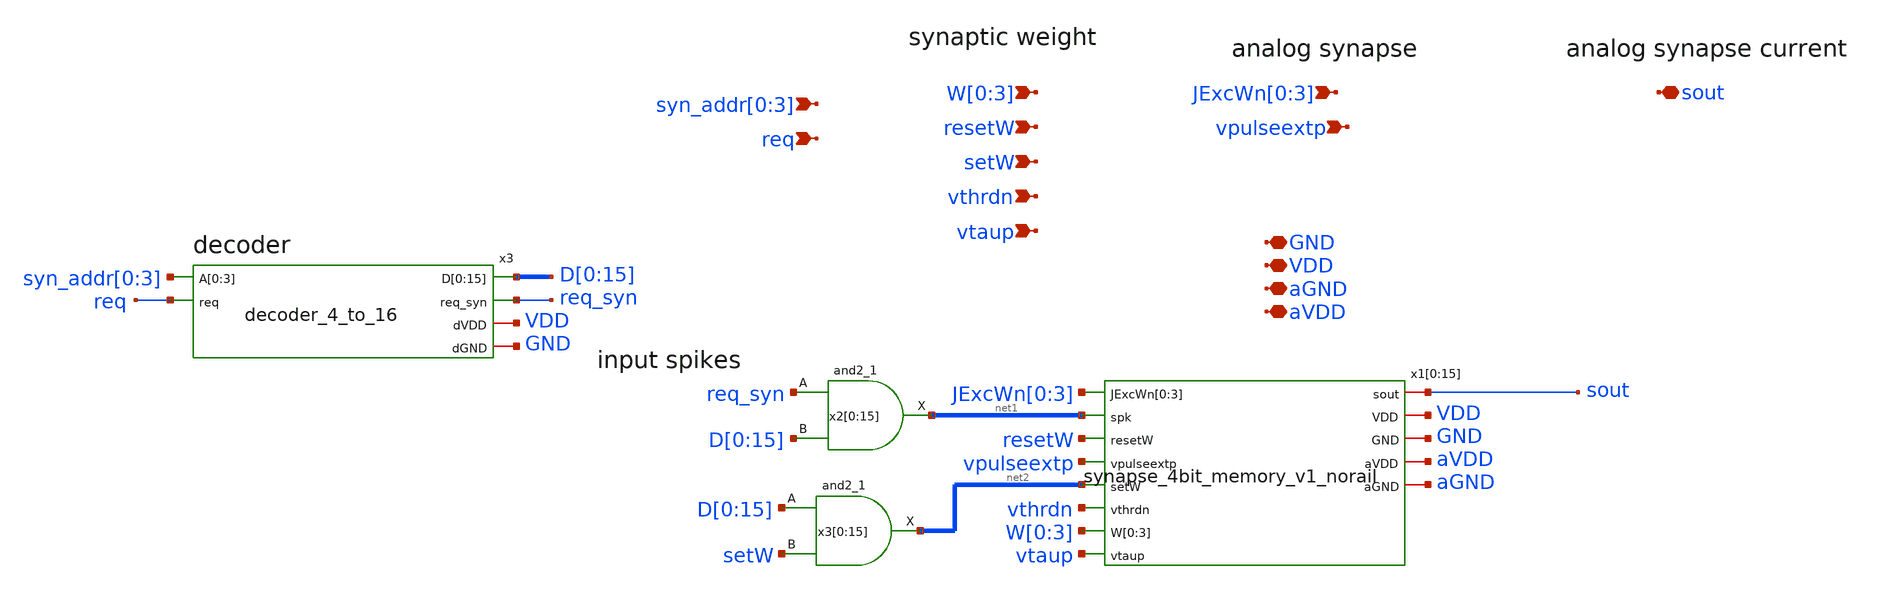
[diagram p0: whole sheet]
** sch_path: design/xschem/synapse_array_programmable_16_to_sout_v1.sch
**.subckt synapse_array_programmable_16_to_sout_v1 GND VDD vpulseextp
*+ syn_addr[0],syn_addr[1],syn_addr[2],syn_addr[3] W[0],W[1],W[2],W[3] JExcWn[0],JExcWn[1],JExcWn[2],JExcWn[3] sout setW resetW req vthrdn vtaup aVDD
*+ aGND
*.iopin GND
*.iopin VDD
*.ipin vpulseextp
*.ipin syn_addr[0],syn_addr[1],syn_addr[2],syn_addr[3]
*.ipin W[0],W[1],W[2],W[3]
*.ipin JExcWn[0],JExcWn[1],JExcWn[2],JExcWn[3]
*.iopin sout
*.ipin setW
*.ipin resetW
*.ipin req
*.ipin vthrdn
*.ipin vtaup
*.iopin aVDD
*.iopin aGND
x3 syn_addr[0] syn_addr[1] syn_addr[2] syn_addr[3] D[0] D[1] D[2] D[3] D[4] D[5] D[6] D[7] D[8] D[9]
+ D[10] D[11] D[12] D[13] D[14] D[15] req req_syn VDD GND decoder_4_to_16
x2[0] req_syn D[0] GND GND VDD VDD net1[15] sky130_fd_sc_hd__and2_1
x2[1] req_syn D[1] GND GND VDD VDD net1[14] sky130_fd_sc_hd__and2_1
x2[2] req_syn D[2] GND GND VDD VDD net1[13] sky130_fd_sc_hd__and2_1
x2[3] req_syn D[3] GND GND VDD VDD net1[12] sky130_fd_sc_hd__and2_1
x2[4] req_syn D[4] GND GND VDD VDD net1[11] sky130_fd_sc_hd__and2_1
x2[5] req_syn D[5] GND GND VDD VDD net1[10] sky130_fd_sc_hd__and2_1
x2[6] req_syn D[6] GND GND VDD VDD net1[9] sky130_fd_sc_hd__and2_1
x2[7] req_syn D[7] GND GND VDD VDD net1[8] sky130_fd_sc_hd__and2_1
x2[8] req_syn D[8] GND GND VDD VDD net1[7] sky130_fd_sc_hd__and2_1
x2[9] req_syn D[9] GND GND VDD VDD net1[6] sky130_fd_sc_hd__and2_1
x2[10] req_syn D[10] GND GND VDD VDD net1[5] sky130_fd_sc_hd__and2_1
x2[11] req_syn D[11] GND GND VDD VDD net1[4] sky130_fd_sc_hd__and2_1
x2[12] req_syn D[12] GND GND VDD VDD net1[3] sky130_fd_sc_hd__and2_1
x2[13] req_syn D[13] GND GND VDD VDD net1[2] sky130_fd_sc_hd__and2_1
x2[14] req_syn D[14] GND GND VDD VDD net1[1] sky130_fd_sc_hd__and2_1
x2[15] req_syn D[15] GND GND VDD VDD net1[0] sky130_fd_sc_hd__and2_1
x1[0] sout JExcWn[0] JExcWn[1] JExcWn[2] JExcWn[3] net1[15] resetW vpulseextp net2[15] vthrdn W[0]
+ W[1] W[2] W[3] vtaup VDD GND aVDD aGND synapse_4bit_memory_v1_norail
x1[1] sout JExcWn[0] JExcWn[1] JExcWn[2] JExcWn[3] net1[14] resetW vpulseextp net2[14] vthrdn W[0]
+ W[1] W[2] W[3] vtaup VDD GND aVDD aGND synapse_4bit_memory_v1_norail
x1[2] sout JExcWn[0] JExcWn[1] JExcWn[2] JExcWn[3] net1[13] resetW vpulseextp net2[13] vthrdn W[0]
+ W[1] W[2] W[3] vtaup VDD GND aVDD aGND synapse_4bit_memory_v1_norail
x1[3] sout JExcWn[0] JExcWn[1] JExcWn[2] JExcWn[3] net1[12] resetW vpulseextp net2[12] vthrdn W[0]
+ W[1] W[2] W[3] vtaup VDD GND aVDD aGND synapse_4bit_memory_v1_norail
x1[4] sout JExcWn[0] JExcWn[1] JExcWn[2] JExcWn[3] net1[11] resetW vpulseextp net2[11] vthrdn W[0]
+ W[1] W[2] W[3] vtaup VDD GND aVDD aGND synapse_4bit_memory_v1_norail
x1[5] sout JExcWn[0] JExcWn[1] JExcWn[2] JExcWn[3] net1[10] resetW vpulseextp net2[10] vthrdn W[0]
+ W[1] W[2] W[3] vtaup VDD GND aVDD aGND synapse_4bit_memory_v1_norail
x1[6] sout JExcWn[0] JExcWn[1] JExcWn[2] JExcWn[3] net1[9] resetW vpulseextp net2[9] vthrdn W[0]
+ W[1] W[2] W[3] vtaup VDD GND aVDD aGND synapse_4bit_memory_v1_norail
x1[7] sout JExcWn[0] JExcWn[1] JExcWn[2] JExcWn[3] net1[8] resetW vpulseextp net2[8] vthrdn W[0]
+ W[1] W[2] W[3] vtaup VDD GND aVDD aGND synapse_4bit_memory_v1_norail
x1[8] sout JExcWn[0] JExcWn[1] JExcWn[2] JExcWn[3] net1[7] resetW vpulseextp net2[7] vthrdn W[0]
+ W[1] W[2] W[3] vtaup VDD GND aVDD aGND synapse_4bit_memory_v1_norail
x1[9] sout JExcWn[0] JExcWn[1] JExcWn[2] JExcWn[3] net1[6] resetW vpulseextp net2[6] vthrdn W[0]
+ W[1] W[2] W[3] vtaup VDD GND aVDD aGND synapse_4bit_memory_v1_norail
x1[10] sout JExcWn[0] JExcWn[1] JExcWn[2] JExcWn[3] net1[5] resetW vpulseextp net2[5] vthrdn W[0]
+ W[1] W[2] W[3] vtaup VDD GND aVDD aGND synapse_4bit_memory_v1_norail
x1[11] sout JExcWn[0] JExcWn[1] JExcWn[2] JExcWn[3] net1[4] resetW vpulseextp net2[4] vthrdn W[0]
+ W[1] W[2] W[3] vtaup VDD GND aVDD aGND synapse_4bit_memory_v1_norail
x1[12] sout JExcWn[0] JExcWn[1] JExcWn[2] JExcWn[3] net1[3] resetW vpulseextp net2[3] vthrdn W[0]
+ W[1] W[2] W[3] vtaup VDD GND aVDD aGND synapse_4bit_memory_v1_norail
x1[13] sout JExcWn[0] JExcWn[1] JExcWn[2] JExcWn[3] net1[2] resetW vpulseextp net2[2] vthrdn W[0]
+ W[1] W[2] W[3] vtaup VDD GND aVDD aGND synapse_4bit_memory_v1_norail
x1[14] sout JExcWn[0] JExcWn[1] JExcWn[2] JExcWn[3] net1[1] resetW vpulseextp net2[1] vthrdn W[0]
+ W[1] W[2] W[3] vtaup VDD GND aVDD aGND synapse_4bit_memory_v1_norail
x1[15] sout JExcWn[0] JExcWn[1] JExcWn[2] JExcWn[3] net1[0] resetW vpulseextp net2[0] vthrdn W[0]
+ W[1] W[2] W[3] vtaup VDD GND aVDD aGND synapse_4bit_memory_v1_norail
x3[0] D[0] setW GND GND VDD VDD net2[15] sky130_fd_sc_hd__and2_1
x3[1] D[1] setW GND GND VDD VDD net2[14] sky130_fd_sc_hd__and2_1
x3[2] D[2] setW GND GND VDD VDD net2[13] sky130_fd_sc_hd__and2_1
x3[3] D[3] setW GND GND VDD VDD net2[12] sky130_fd_sc_hd__and2_1
x3[4] D[4] setW GND GND VDD VDD net2[11] sky130_fd_sc_hd__and2_1
x3[5] D[5] setW GND GND VDD VDD net2[10] sky130_fd_sc_hd__and2_1
x3[6] D[6] setW GND GND VDD VDD net2[9] sky130_fd_sc_hd__and2_1
x3[7] D[7] setW GND GND VDD VDD net2[8] sky130_fd_sc_hd__and2_1
x3[8] D[8] setW GND GND VDD VDD net2[7] sky130_fd_sc_hd__and2_1
x3[9] D[9] setW GND GND VDD VDD net2[6] sky130_fd_sc_hd__and2_1
x3[10] D[10] setW GND GND VDD VDD net2[5] sky130_fd_sc_hd__and2_1
x3[11] D[11] setW GND GND VDD VDD net2[4] sky130_fd_sc_hd__and2_1
x3[12] D[12] setW GND GND VDD VDD net2[3] sky130_fd_sc_hd__and2_1
x3[13] D[13] setW GND GND VDD VDD net2[2] sky130_fd_sc_hd__and2_1
x3[14] D[14] setW GND GND VDD VDD net2[1] sky130_fd_sc_hd__and2_1
x3[15] D[15] setW GND GND VDD VDD net2[0] sky130_fd_sc_hd__and2_1
**.ends

* expanding   symbol:  decoder_4_to_16.sym # of pins=6
** sym_path: design/xschem/decoder_4_to_16.sym
** sch_path: design/xschem/decoder_4_to_16.sch
.subckt decoder_4_to_16 A[0] A[1] A[2] A[3] D[0] D[1] D[2] D[3] D[4] D[5] D[6] D[7] D[8] D[9] D[10]
+ D[11] D[12] D[13] D[14] D[15] req req_syn dVDD dGND
*.ipin A[0],A[1],A[2],A[3]
*.ipin req
*.opin D[0],D[1],D[2],D[3],D[4],D[5],D[6],D[7],D[8],D[9],D[10],D[11],D[12],D[13],D[14],D[15]
*.opin req_syn
*.iopin dVDD
*.iopin dGND
x21 req dGND dGND dVDD dVDD net5 sky130_fd_sc_hd__inv_1
x22 net5 dGND dGND dVDD dVDD net6 sky130_fd_sc_hd__inv_1
x23 net6 dGND dGND dVDD dVDD net7 sky130_fd_sc_hd__inv_1
x24 net7 dGND dGND dVDD dVDD req_syn sky130_fd_sc_hd__inv_1
x20 A[3] A[2] A[1] A[0] dGND dGND dVDD dVDD D[15] sky130_fd_sc_hd__and4_1
x19 A[3] A[2] A[1] net4 dGND dGND dVDD dVDD D[14] sky130_fd_sc_hd__and4_1
x18 A[3] A[2] net3 A[0] dGND dGND dVDD dVDD D[13] sky130_fd_sc_hd__and4_1
x17 A[3] A[2] net3 net4 dGND dGND dVDD dVDD D[12] sky130_fd_sc_hd__and4_1
x16 A[3] net2 A[1] A[0] dGND dGND dVDD dVDD D[11] sky130_fd_sc_hd__and4_1
x15 A[3] net2 A[1] net4 dGND dGND dVDD dVDD D[10] sky130_fd_sc_hd__and4_1
x13 A[3] net2 net3 A[0] dGND dGND dVDD dVDD D[9] sky130_fd_sc_hd__and4_1
x4 A[3] net2 net3 net4 dGND dGND dVDD dVDD D[8] sky130_fd_sc_hd__and4_1
x5 net1 A[2] A[1] A[0] dGND dGND dVDD dVDD D[7] sky130_fd_sc_hd__and4_1
x6 net1 A[2] A[1] net4 dGND dGND dVDD dVDD D[6] sky130_fd_sc_hd__and4_1
x8 net1 A[2] net3 net4 dGND dGND dVDD dVDD D[4] sky130_fd_sc_hd__and4_1
x9 net1 net2 A[1] net4 dGND dGND dVDD dVDD D[2] sky130_fd_sc_hd__and4_1
x10 net1 net2 net3 net4 dGND dGND dVDD dVDD D[0] sky130_fd_sc_hd__and4_1
x11 net1 net2 net3 A[0] dGND dGND dVDD dVDD D[1] sky130_fd_sc_hd__and4_1
x12 net1 net2 A[1] A[0] dGND dGND dVDD dVDD D[3] sky130_fd_sc_hd__and4_1
x14 net1 A[2] net3 A[0] dGND dGND dVDD dVDD D[5] sky130_fd_sc_hd__and4_1
x1 A[3] dGND dGND dVDD dVDD net1 sky130_fd_sc_hd__inv_4
x2 A[2] dGND dGND dVDD dVDD net2 sky130_fd_sc_hd__inv_4
x3 A[1] dGND dGND dVDD dVDD net3 sky130_fd_sc_hd__inv_4
x7 A[0] dGND dGND dVDD dVDD net4 sky130_fd_sc_hd__inv_4
.ends


* expanding   symbol:  synapse_4bit_memory_v1_norail.sym # of pins=13
** sym_path: design/xschem/synapse_4bit_memory_v1_norail.sym
** sch_path: design/xschem/synapse_4bit_memory_v1_norail.sch
.subckt synapse_4bit_memory_v1_norail sout JExcWn[0] JExcWn[1] JExcWn[2] JExcWn[3] spk resetW
+ vpulseextp setW vthrdn W[0] W[1] W[2] W[3] vtaup VDD GND aVDD aGND
*.iopin GND
*.iopin VDD
*.ipin vpulseextp
*.ipin spk
*.ipin setW
*.ipin resetW
*.iopin sout
*.ipin vthrdn
*.ipin vtaup
*.iopin aVDD
*.ipin JExcWn[0],JExcWn[1],JExcWn[2],JExcWn[3]
*.ipin W[0],W[1],W[2],W[3]
*.iopin aGND
x2[0] setW W[0] net1 GND GND VDD VDD net2[3] sky130_fd_sc_hd__dfrtp_1
x2[1] setW W[1] net1 GND GND VDD VDD net2[2] sky130_fd_sc_hd__dfrtp_1
x2[2] setW W[2] net1 GND GND VDD VDD net2[1] sky130_fd_sc_hd__dfrtp_1
x2[3] setW W[3] net1 GND GND VDD VDD net2[0] sky130_fd_sc_hd__dfrtp_1
x4 resetW GND GND VDD VDD net1 sky130_fd_sc_hd__inv_1
x2 vtaup sout vthrdn spke JExcWn[0] JExcWn[1] JExcWn[2] JExcWn[3] aGND aVDD net2[3] net2[2] net2[1]
+ net2[0] dpi_syn_exc_4bit_fc_v2
x6 vpulseextp spk GND spke VDD spike_extender_with_trimming
x1 GND GND VDD VDD sky130_fd_sc_hd__decap_4
x3 GND GND VDD VDD sky130_fd_sc_hd__decap_3
x5 GND GND VDD VDD sky130_fd_sc_hd__decap_3
x7 GND GND VDD VDD sky130_fd_sc_hd__decap_6
x8 GND GND VDD VDD sky130_fd_sc_hd__decap_3
x9 GND GND VDD VDD sky130_fd_sc_hd__decap_3
.ends


* expanding   symbol:  dpi_syn_exc_4bit_fc_v2.sym # of pins=8
** sym_path: design/xschem/dpi_syn_exc_4bit_fc_v2.sym
** sch_path: design/xschem/dpi_syn_exc_4bit_fc_v2.sch
.subckt dpi_syn_exc_4bit_fc_v2 vtaup sout vthn spk JExcWn[0] JExcWn[1] JExcWn[2] JExcWn[3] GND aVDD
+ weight[0] weight[1] weight[2] weight[3]
*.iopin GND
*.iopin aVDD
*.iopin vtaup
*.ipin spk
*.opin sout
*.iopin vthn
*.ipin weight[0],weight[1],weight[2],weight[3]
*.iopin JExcWn[0],JExcWn[1],JExcWn[2],JExcWn[3]
XM2 net3 spk net1 GND sky130_fd_pr__nfet_01v8 L=0.25 W=1.0 nf=1 ad='int((nf+1)/2) * W/nf * 0.29' as='int((nf+2)/2) * W/nf * 0.29'
+ pd='2*int((nf+1)/2) * (W/nf + 0.29)' ps='2*int((nf+2)/2) * (W/nf + 0.29)' nrd='0.29 / W' nrs='0.29 / W'
+ sa=0 sb=0 sd=0 mult=1 m=1
XC1 vsin aVDD sky130_fd_pr__cap_mim_m3_1 W=5 L=5 MF=1 m=1
XM5 vsin vtaup aVDD aVDD sky130_fd_pr__pfet_01v8 L=0.2 W=1.2 nf=1 ad='int((nf+1)/2) * W/nf * 0.29' as='int((nf+2)/2) * W/nf * 0.29'
+ pd='2*int((nf+1)/2) * (W/nf + 0.29)' ps='2*int((nf+2)/2) * (W/nf + 0.29)' nrd='0.29 / W' nrs='0.29 / W'
+ sa=0 sb=0 sd=0 mult=1 m=1
XM6 sout vsin aVDD aVDD sky130_fd_pr__pfet_01v8 L=0.2 W=1.2 nf=1 ad='int((nf+1)/2) * W/nf * 0.29' as='int((nf+2)/2) * W/nf * 0.29'
+ pd='2*int((nf+1)/2) * (W/nf + 0.29)' ps='2*int((nf+2)/2) * (W/nf + 0.29)' nrd='0.29 / W' nrs='0.29 / W'
+ sa=0 sb=0 sd=0 mult=1 m=1
XM1 net1 JExcWn[0] net2 GND sky130_fd_pr__nfet_01v8 L=1.0 W=1.0 nf=1 ad='int((nf+1)/2) * W/nf * 0.29'
+ as='int((nf+2)/2) * W/nf * 0.29' pd='2*int((nf+1)/2) * (W/nf + 0.29)' ps='2*int((nf+2)/2) * (W/nf + 0.29)'
+ nrd='0.29 / W' nrs='0.29 / W' sa=0 sb=0 sd=0 mult=1 m=1
XM4 vsin vsin net3 GND sky130_fd_pr__nfet_01v8 L=0.25 W=1.0 nf=1 ad='int((nf+1)/2) * W/nf * 0.29' as='int((nf+2)/2) * W/nf * 0.29'
+ pd='2*int((nf+1)/2) * (W/nf + 0.29)' ps='2*int((nf+2)/2) * (W/nf + 0.29)' nrd='0.29 / W' nrs='0.29 / W'
+ sa=0 sb=0 sd=0 mult=1 m=1
XM3 aVDD vthn net3 GND sky130_fd_pr__nfet_01v8 L=0.25 W=1.0 nf=1 ad='int((nf+1)/2) * W/nf * 0.29' as='int((nf+2)/2) * W/nf * 0.29'
+ pd='2*int((nf+1)/2) * (W/nf + 0.29)' ps='2*int((nf+2)/2) * (W/nf + 0.29)' nrd='0.29 / W' nrs='0.29 / W'
+ sa=0 sb=0 sd=0 mult=1 m=1
XM7 net1 JExcWn[1] net4 GND sky130_fd_pr__nfet_01v8 L=2.0 W=1.0 nf=1 ad='int((nf+1)/2) * W/nf * 0.29'
+ as='int((nf+2)/2) * W/nf * 0.29' pd='2*int((nf+1)/2) * (W/nf + 0.29)' ps='2*int((nf+2)/2) * (W/nf + 0.29)'
+ nrd='0.29 / W' nrs='0.29 / W' sa=0 sb=0 sd=0 mult=1 m=1
XM8 net1 JExcWn[2] net5 GND sky130_fd_pr__nfet_01v8 L=4.0 W=1.0 nf=1 ad='int((nf+1)/2) * W/nf * 0.29'
+ as='int((nf+2)/2) * W/nf * 0.29' pd='2*int((nf+1)/2) * (W/nf + 0.29)' ps='2*int((nf+2)/2) * (W/nf + 0.29)'
+ nrd='0.29 / W' nrs='0.29 / W' sa=0 sb=0 sd=0 mult=1 m=1
XM9 net1 JExcWn[3] net6 GND sky130_fd_pr__nfet_01v8 L=8.0 W=1.0 nf=1 ad='int((nf+1)/2) * W/nf * 0.29'
+ as='int((nf+2)/2) * W/nf * 0.29' pd='2*int((nf+1)/2) * (W/nf + 0.29)' ps='2*int((nf+2)/2) * (W/nf + 0.29)'
+ nrd='0.29 / W' nrs='0.29 / W' sa=0 sb=0 sd=0 mult=1 m=1
XM10 net2 weight[0] GND GND sky130_fd_pr__nfet_01v8 L=0.25 W=1.0 nf=1 ad='int((nf+1)/2) * W/nf * 0.29'
+ as='int((nf+2)/2) * W/nf * 0.29' pd='2*int((nf+1)/2) * (W/nf + 0.29)' ps='2*int((nf+2)/2) * (W/nf + 0.29)'
+ nrd='0.29 / W' nrs='0.29 / W' sa=0 sb=0 sd=0 mult=1 m=1
XM11 net4 weight[1] GND GND sky130_fd_pr__nfet_01v8 L=0.25 W=1.0 nf=1 ad='int((nf+1)/2) * W/nf * 0.29'
+ as='int((nf+2)/2) * W/nf * 0.29' pd='2*int((nf+1)/2) * (W/nf + 0.29)' ps='2*int((nf+2)/2) * (W/nf + 0.29)'
+ nrd='0.29 / W' nrs='0.29 / W' sa=0 sb=0 sd=0 mult=1 m=1
XM12 net5 weight[2] GND GND sky130_fd_pr__nfet_01v8 L=0.25 W=1.0 nf=1 ad='int((nf+1)/2) * W/nf * 0.29'
+ as='int((nf+2)/2) * W/nf * 0.29' pd='2*int((nf+1)/2) * (W/nf + 0.29)' ps='2*int((nf+2)/2) * (W/nf + 0.29)'
+ nrd='0.29 / W' nrs='0.29 / W' sa=0 sb=0 sd=0 mult=1 m=1
XM13 net6 weight[3] GND GND sky130_fd_pr__nfet_01v8 L=0.25 W=1.0 nf=1 ad='int((nf+1)/2) * W/nf * 0.29'
+ as='int((nf+2)/2) * W/nf * 0.29' pd='2*int((nf+1)/2) * (W/nf + 0.29)' ps='2*int((nf+2)/2) * (W/nf + 0.29)'
+ nrd='0.29 / W' nrs='0.29 / W' sa=0 sb=0 sd=0 mult=1 m=1
.ends


* expanding   symbol:  spike_extender_with_trimming.sym # of pins=5
** sym_path: design/xschem/spike_extender_with_trimming.sym
** sch_path: design/xschem/spike_extender_with_trimming.sch
.subckt spike_extender_with_trimming vpulseextp vspk GND spkext VDD
*.iopin GND
*.iopin VDD
*.ipin vspk
*.opin spkext
*.ipin vpulseextp
x1 vpulseextp vpulseshort GND spkext VDD spike_extender
x3 vspk GND GND VDD VDD net1 sky130_fd_sc_hd__clkdlybuf4s50_1
x2 net1 vspk GND GND VDD VDD vpulseshort sky130_fd_sc_hd__nor2b_1
.ends


* expanding   symbol:  spike_extender.sym # of pins=5
** sym_path: design/xschem/spike_extender.sym
** sch_path: design/xschem/spike_extender.sch
.subckt spike_extender vpulseextp spk GND spkext VDD
*.iopin GND
*.iopin VDD
*.ipin spk
*.opin spkext
*.ipin vpulseextp
XM1 net1 spk GND GND sky130_fd_pr__nfet_01v8 L=0.15 W=0.65 nf=1 ad='int((nf+1)/2) * W/nf * 0.29' as='int((nf+2)/2) * W/nf * 0.29'
+ pd='2*int((nf+1)/2) * (W/nf + 0.29)' ps='2*int((nf+2)/2) * (W/nf + 0.29)' nrd='0.29 / W' nrs='0.29 / W'
+ sa=0 sb=0 sd=0 mult=1 m=1
XM6 net1 vpulseextp VDD VDD sky130_fd_pr__pfet_01v8 L=2 W=1 nf=1 ad='int((nf+1)/2) * W/nf * 0.29' as='int((nf+2)/2) * W/nf * 0.29'
+ pd='2*int((nf+1)/2) * (W/nf + 0.29)' ps='2*int((nf+2)/2) * (W/nf + 0.29)' nrd='0.29 / W' nrs='0.29 / W'
+ sa=0 sb=0 sd=0 mult=1 m=1
XM5 net3 net2 GND GND sky130_fd_pr__nfet_01v8 L=0.15 W=0.65 nf=1 ad='int((nf+1)/2) * W/nf * 0.29' as='int((nf+2)/2) * W/nf * 0.29'
+ pd='2*int((nf+1)/2) * (W/nf + 0.29)' ps='2*int((nf+2)/2) * (W/nf + 0.29)' nrd='0.29 / W' nrs='0.29 / W'
+ sa=0 sb=0 sd=0 mult=1 m=1
XM8 spkext net3 GND GND sky130_fd_pr__nfet_01v8 L=0.15 W=0.65 nf=1 ad='int((nf+1)/2) * W/nf * 0.29' as='int((nf+2)/2) * W/nf * 0.29'
+ pd='2*int((nf+1)/2) * (W/nf + 0.29)' ps='2*int((nf+2)/2) * (W/nf + 0.29)' nrd='0.29 / W' nrs='0.29 / W'
+ sa=0 sb=0 sd=0 mult=1 m=1
XM4 net3 net2 VDD VDD sky130_fd_pr__pfet_01v8 L=0.15 W=1.0 nf=1 ad='int((nf+1)/2) * W/nf * 0.29' as='int((nf+2)/2) * W/nf * 0.29'
+ pd='2*int((nf+1)/2) * (W/nf + 0.29)' ps='2*int((nf+2)/2) * (W/nf + 0.29)' nrd='0.29 / W' nrs='0.29 / W'
+ sa=0 sb=0 sd=0 mult=1 m=1
XM7 spkext net3 VDD VDD sky130_fd_pr__pfet_01v8 L=0.15 W=1.0 nf=1 ad='int((nf+1)/2) * W/nf * 0.29' as='int((nf+2)/2) * W/nf * 0.29'
+ pd='2*int((nf+1)/2) * (W/nf + 0.29)' ps='2*int((nf+2)/2) * (W/nf + 0.29)' nrd='0.29 / W' nrs='0.29 / W'
+ sa=0 sb=0 sd=0 mult=1 m=1
XM2 net2 net1 GND GND sky130_fd_pr__nfet_01v8 L=0.15 W=0.65 nf=1 ad='int((nf+1)/2) * W/nf * 0.29' as='int((nf+2)/2) * W/nf * 0.29'
+ pd='2*int((nf+1)/2) * (W/nf + 0.29)' ps='2*int((nf+2)/2) * (W/nf + 0.29)' nrd='0.29 / W' nrs='0.29 / W'
+ sa=0 sb=0 sd=0 mult=1 m=1
XM3 net2 net1 VDD VDD sky130_fd_pr__pfet_01v8 L=0.15 W=1.0 nf=1 ad='int((nf+1)/2) * W/nf * 0.29' as='int((nf+2)/2) * W/nf * 0.29'
+ pd='2*int((nf+1)/2) * (W/nf + 0.29)' ps='2*int((nf+2)/2) * (W/nf + 0.29)' nrd='0.29 / W' nrs='0.29 / W'
+ sa=0 sb=0 sd=0 mult=1 m=1
XM9 GND net1 GND GND sky130_fd_pr__nfet_01v8 L=1 W=0.65 nf=1 ad='int((nf+1)/2) * W/nf * 0.29' as='int((nf+2)/2) * W/nf * 0.29'
+ pd='2*int((nf+1)/2) * (W/nf + 0.29)' ps='2*int((nf+2)/2) * (W/nf + 0.29)' nrd='0.29 / W' nrs='0.29 / W'
+ sa=0 sb=0 sd=0 mult=1 m=1
.ends

.end
